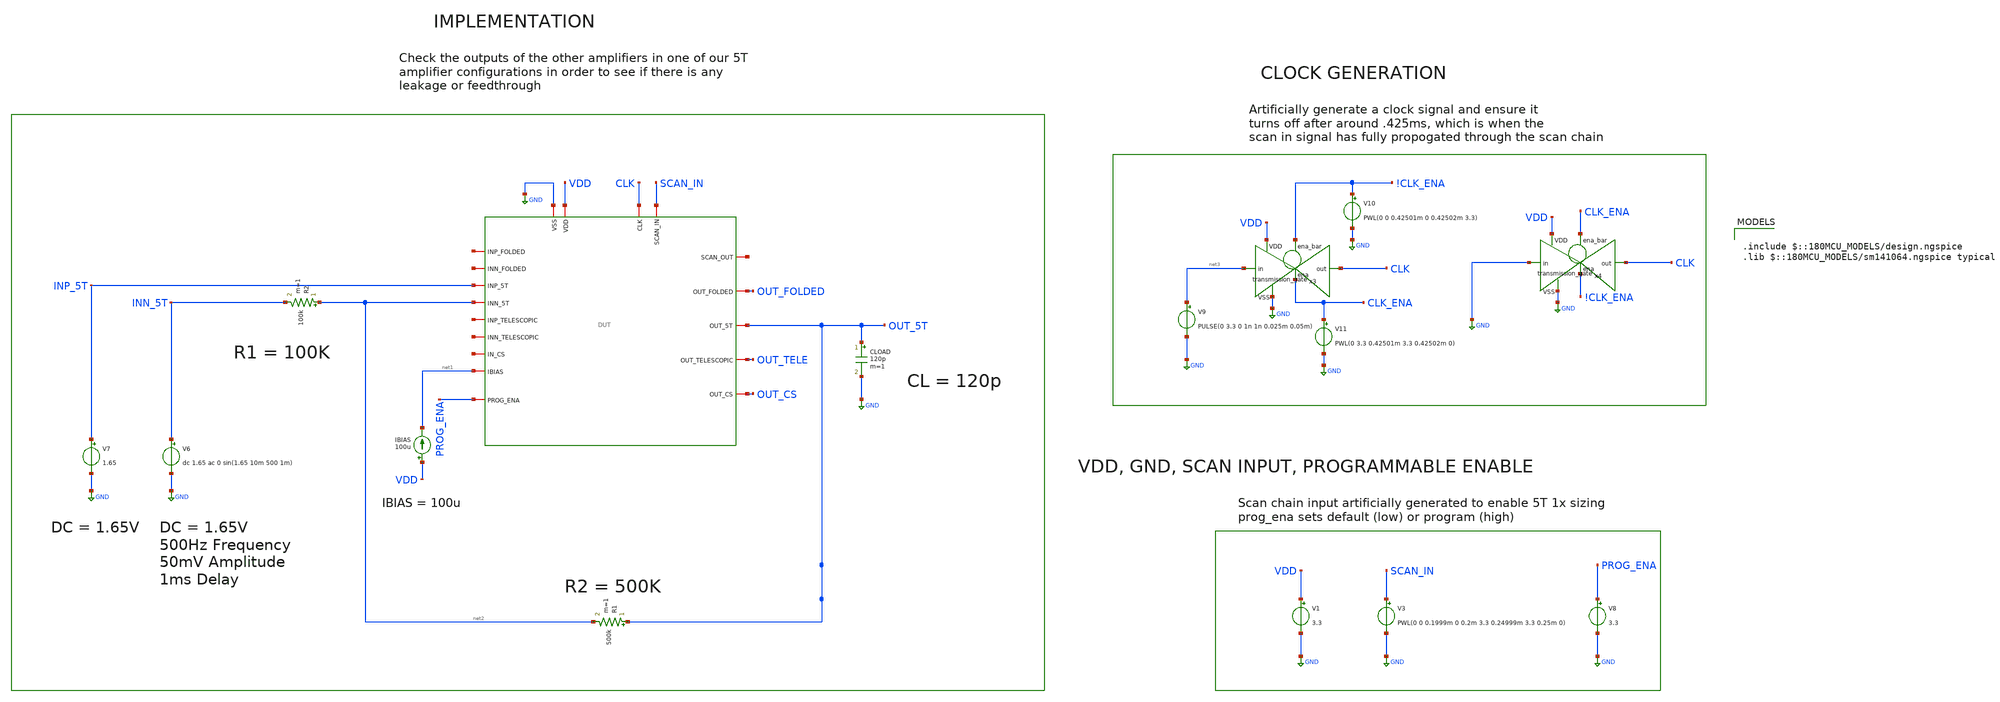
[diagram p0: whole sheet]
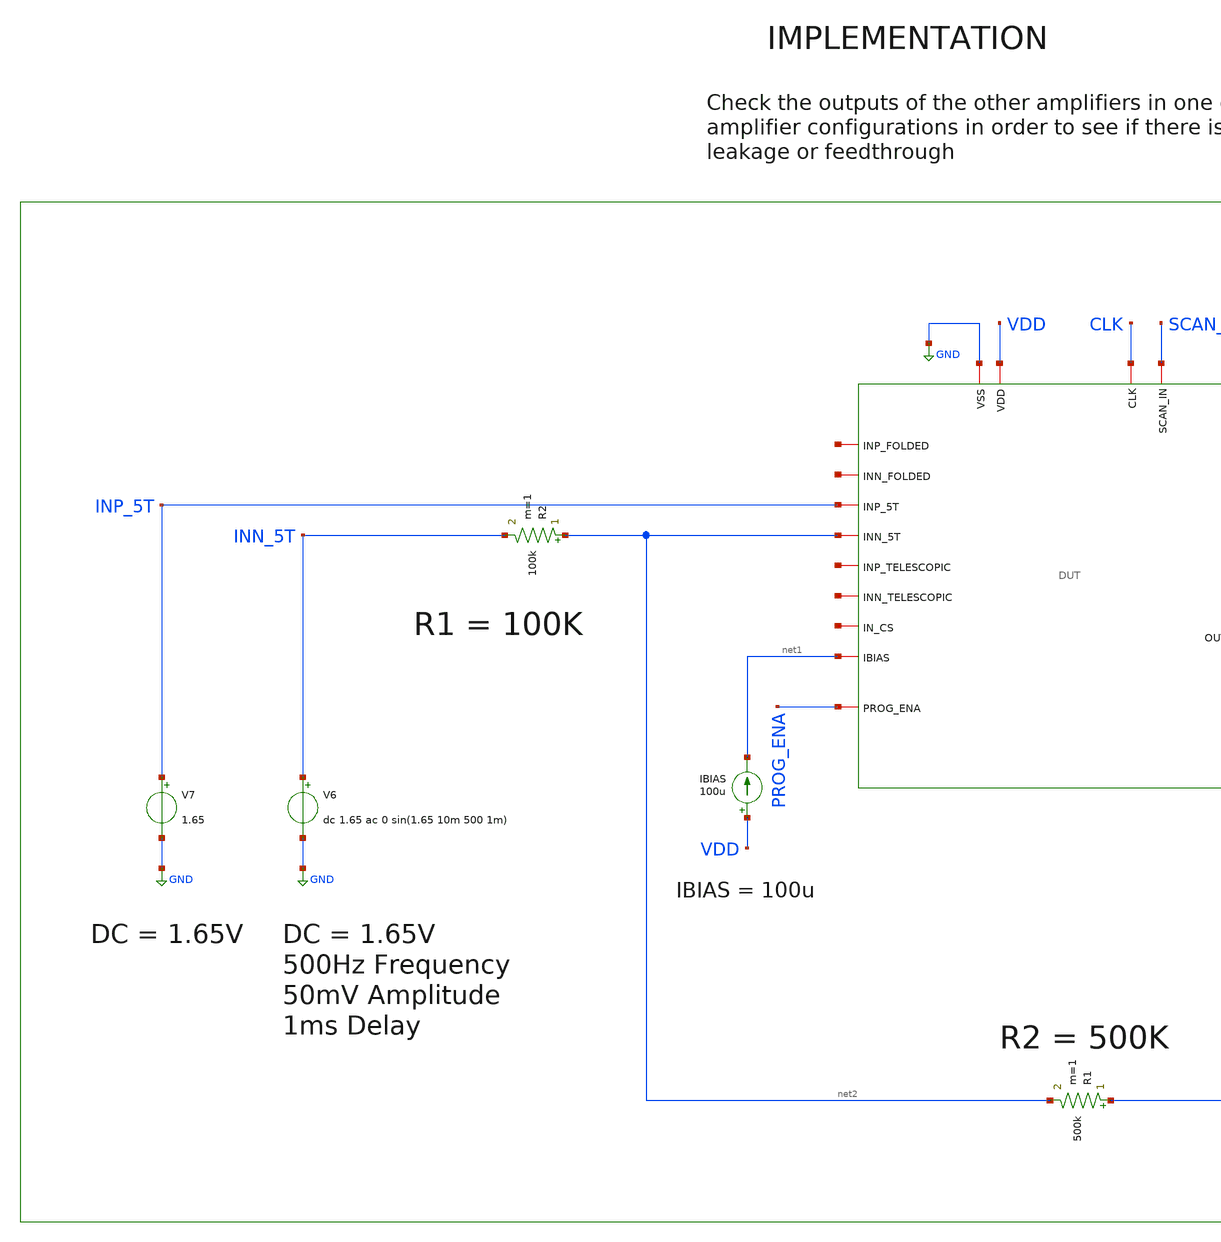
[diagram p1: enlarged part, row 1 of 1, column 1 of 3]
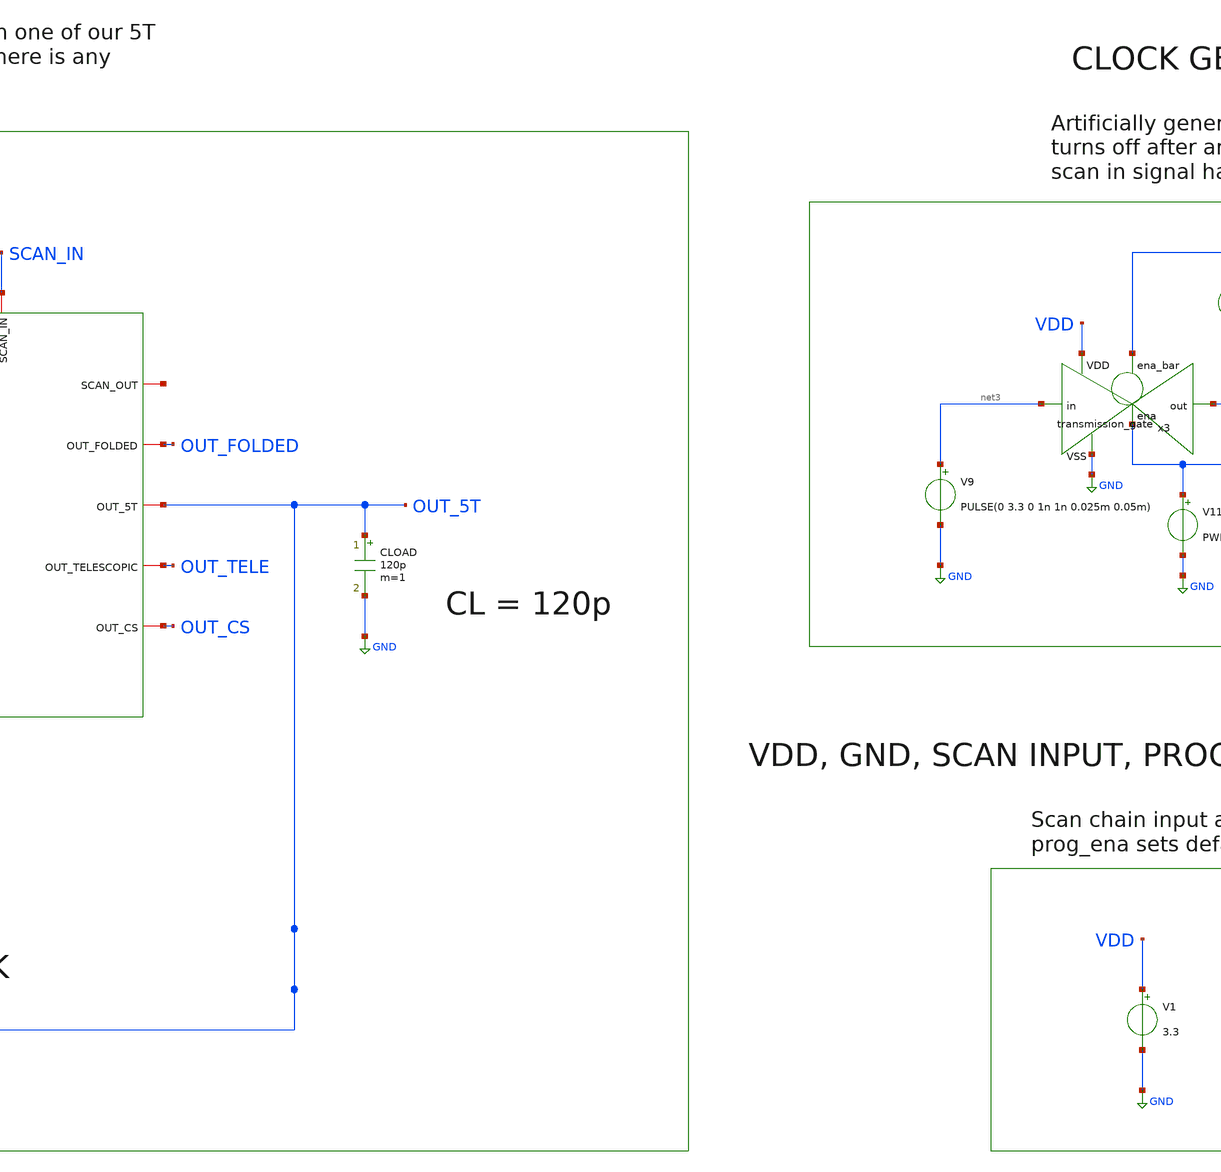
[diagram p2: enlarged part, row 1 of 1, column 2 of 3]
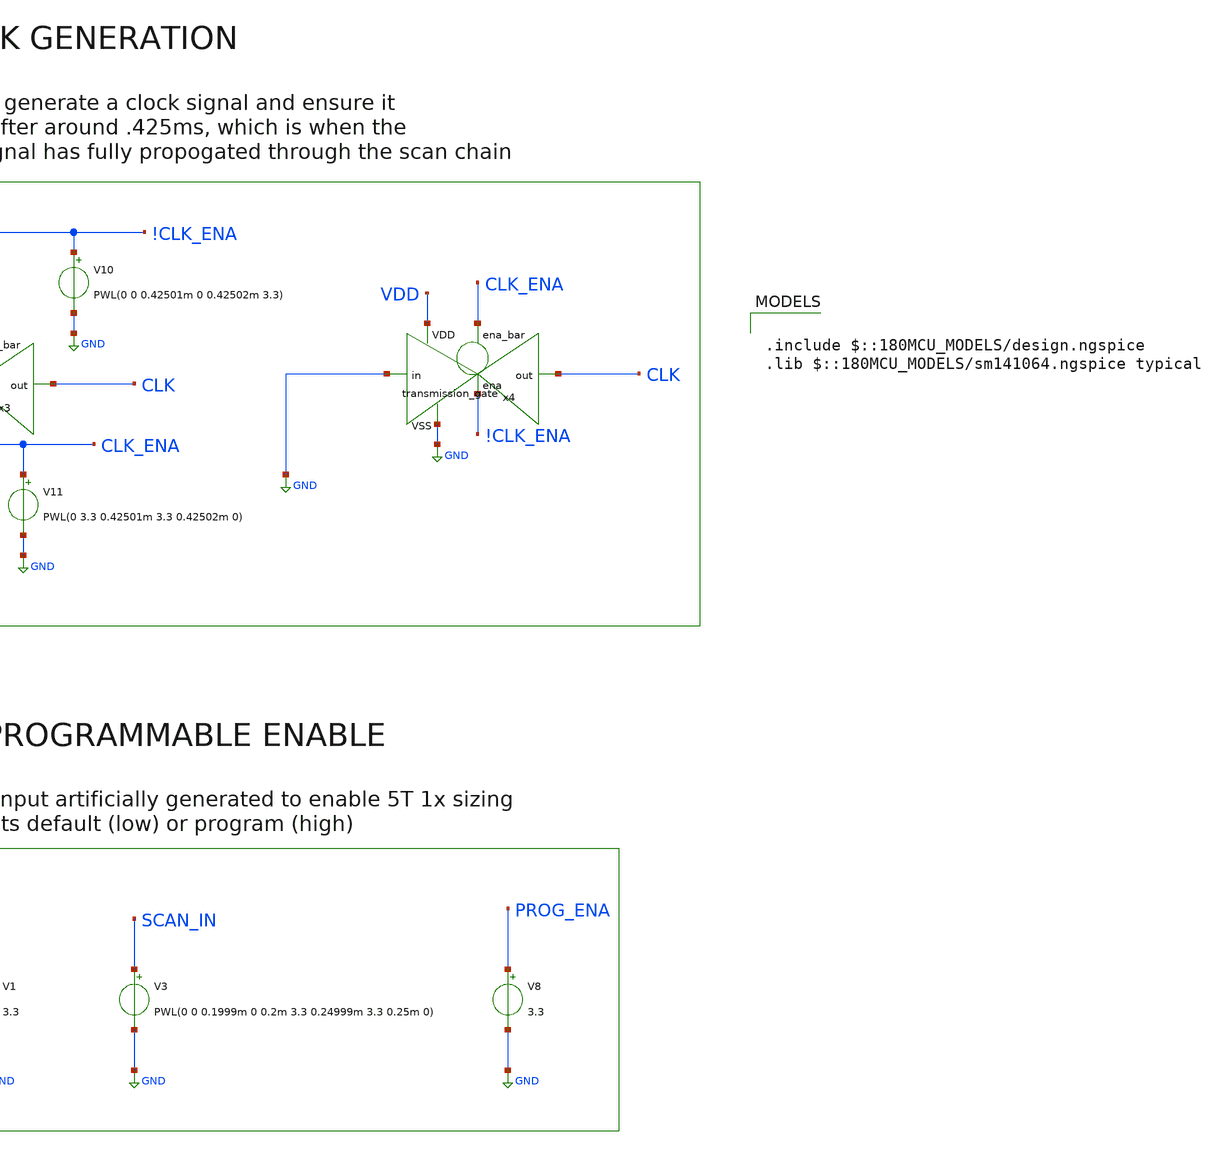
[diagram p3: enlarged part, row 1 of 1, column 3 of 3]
** sch_path: designs/libs/verification/ota_5t/output_isolation/output_isolation_tb.sch
**.subckt output_isolation_tb
V3 SCAN_IN GND PWL(0 0 0.1999m 0 0.2m 3.3 0.24999m 3.3 0.25m 0)
V1 VDD GND 3.3
IBIAS VDD net1 100u
V7 INP_5T GND 1.65
CLOAD OUT_5T GND 120p m=1
R2 net2 INN_5T 100k m=1
V6 INN_5T GND dc 1.65 ac 0 sin(1.65 10m 500 1m)
R1 OUT_5T net2 500k m=1
x1 CLK net4 SCAN_IN GND VDD OUT_FOLDED net5 OUT_5T net1 net6 INP_5T net2 net7 OUT_TELE OUT_CS net8
+ net9 PROG_ENA DUT
V8 PROG_ENA GND 3.3
V9 net3 GND PULSE(0 3.3 0 1n 1n 0.025m 0.05m)
x3 !CLK_ENA VDD CLK net3 GND CLK_ENA transmission_gate
V10 !CLK_ENA GND PWL(0 0 0.42501m 0 0.42502m 3.3)
V11 CLK_ENA GND PWL(0 3.3 0.42501m 3.3 0.42502m 0)
x4 CLK_ENA VDD CLK GND GND !CLK_ENA transmission_gate
**** begin user architecture code

.include $::180MCU_MODELS/design.ngspice
.lib $::180MCU_MODELS/sm141064.ngspice typical



.control
tran 1u 5m

plot v(out_folded) v(out_5t) v(out_tele) v(out_cs)

meas tran folded_pp pp v(out_folded) from=2m to=5m
meas tran five_t_pp pp v(out_5t) from=2m to=5m
meas tran tele_pp pp v(out_tele) from=2m to=5m
meas tran cs_pp pp v(out_cs) from=2m to=5m

print folded_pp five_t_pp tele_pp cs_pp

let iso_folded = 20 * log(five_t_pp / five_t_pp) / log(10)
let iso_tele = 20 * log(tele_pp / five_t_pp) / log(10)
let iso_cs = 20 * log(cs_pp / five_t_pp) / log(10)

print iso_folded iso_tele iso_cs
.endc


**** end user architecture code
**.ends
.GLOBAL GND
.end
